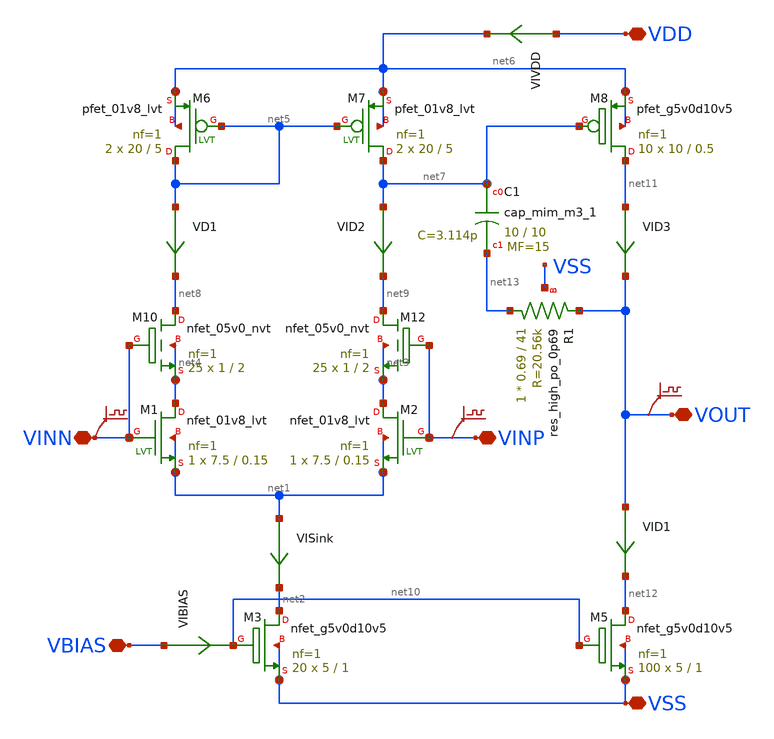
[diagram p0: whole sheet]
** sch_path: xschem/Input_Stage_OA2.sch
**.subckt Input_Stage_OA2 VINN VINP VOUT VDD VSS VBIAS
*.iopin VINN
*.iopin VINP
*.iopin VOUT
*.iopin VDD
*.iopin VSS
*.iopin VBIAS
XM1 net4 VINN net1 net1 sky130_fd_pr__nfet_01v8_lvt L=0.15 W=7.5 nf=1 ad='int((nf+1)/2) * W/nf * 0.29'
+ as='int((nf+2)/2) * W/nf * 0.29' pd='2*int((nf+1)/2) * (W/nf + 0.29)' ps='2*int((nf+2)/2) * (W/nf + 0.29)'
+ nrd='0.29 / W' nrs='0.29 / W' sa=0 sb=0 sd=0 mult=1 m=1
XM2 net3 VINP net1 net1 sky130_fd_pr__nfet_01v8_lvt L=0.15 W=7.5 nf=1 ad='int((nf+1)/2) * W/nf * 0.29'
+ as='int((nf+2)/2) * W/nf * 0.29' pd='2*int((nf+1)/2) * (W/nf + 0.29)' ps='2*int((nf+2)/2) * (W/nf + 0.29)'
+ nrd='0.29 / W' nrs='0.29 / W' sa=0 sb=0 sd=0 mult=1 m=1
VISink net1 net2 0
.save i(visink)
XM6 net5 net5 net6 net6 sky130_fd_pr__pfet_01v8_lvt L=5 W=20 nf=1 ad='int((nf+1)/2) * W/nf * 0.29' as='int((nf+2)/2) * W/nf * 0.29'
+ pd='2*int((nf+1)/2) * (W/nf + 0.29)' ps='2*int((nf+2)/2) * (W/nf + 0.29)' nrd='0.29 / W' nrs='0.29 / W'
+ sa=0 sb=0 sd=0 mult=2 m=2
XM7 net7 net5 net6 net6 sky130_fd_pr__pfet_01v8_lvt L=5 W=20 nf=1 ad='int((nf+1)/2) * W/nf * 0.29' as='int((nf+2)/2) * W/nf * 0.29'
+ pd='2*int((nf+1)/2) * (W/nf + 0.29)' ps='2*int((nf+2)/2) * (W/nf + 0.29)' nrd='0.29 / W' nrs='0.29 / W'
+ sa=0 sb=0 sd=0 mult=2 m=2
VD1 net5 net8 0
.save i(vd1)
VID2 net7 net9 0
.save i(vid2)
VID1 VOUT net12 0
.save i(vid1)
VID3 net11 VOUT 0
.save i(vid3)
.save v(vinn)
.save v(vinp)
.save v(vout)
VIBIAS VBIAS net10 0
.save i(vibias)
XM10 net8 VINN net4 net4 sky130_fd_pr__nfet_05v0_nvt L=2 W=1 nf=1 ad='int((nf+1)/2) * W/nf * 0.29' as='int((nf+2)/2) * W/nf * 0.29'
+ pd='2*int((nf+1)/2) * (W/nf + 0.29)' ps='2*int((nf+2)/2) * (W/nf + 0.29)' nrd='0.29 / W' nrs='0.29 / W'
+ sa=0 sb=0 sd=0 mult=25 m=25
XM12 net9 VINP net3 net3 sky130_fd_pr__nfet_05v0_nvt L=2 W=1 nf=1 ad='int((nf+1)/2) * W/nf * 0.29' as='int((nf+2)/2) * W/nf * 0.29'
+ pd='2*int((nf+1)/2) * (W/nf + 0.29)' ps='2*int((nf+2)/2) * (W/nf + 0.29)' nrd='0.29 / W' nrs='0.29 / W'
+ sa=0 sb=0 sd=0 mult=25 m=25
XM3 net2 net10 VSS VSS sky130_fd_pr__nfet_g5v0d10v5 L=1 W=5 nf=1 ad='int((nf+1)/2) * W/nf * 0.29' as='int((nf+2)/2) * W/nf * 0.29'
+ pd='2*int((nf+1)/2) * (W/nf + 0.29)' ps='2*int((nf+2)/2) * (W/nf + 0.29)' nrd='0.29 / W' nrs='0.29 / W'
+ sa=0 sb=0 sd=0 mult=20 m=20
XM5 net12 net10 VSS VSS sky130_fd_pr__nfet_g5v0d10v5 L=1 W=5 nf=1 ad='int((nf+1)/2) * W/nf * 0.29' as='int((nf+2)/2) * W/nf * 0.29'
+ pd='2*int((nf+1)/2) * (W/nf + 0.29)' ps='2*int((nf+2)/2) * (W/nf + 0.29)' nrd='0.29 / W' nrs='0.29 / W'
+ sa=0 sb=0 sd=0 mult=100 m=100
XM8 net11 net7 net6 net6 sky130_fd_pr__pfet_g5v0d10v5 L=0.5 W=10 nf=1 ad='int((nf+1)/2) * W/nf * 0.29'
+ as='int((nf+2)/2) * W/nf * 0.29' pd='2*int((nf+1)/2) * (W/nf + 0.29)' ps='2*int((nf+2)/2) * (W/nf + 0.29)'
+ nrd='0.29 / W' nrs='0.29 / W' sa=0 sb=0 sd=0 mult=10 m=10
VIVDD VDD net6 0
.save i(vivdd)
XC1 net7 net13 sky130_fd_pr__cap_mim_m3_1 W=10 L=10 MF=15 m=15
XR1 net13 VOUT VSS sky130_fd_pr__res_high_po_0p69 L=41 mult=1 m=1
**.ends
.end
